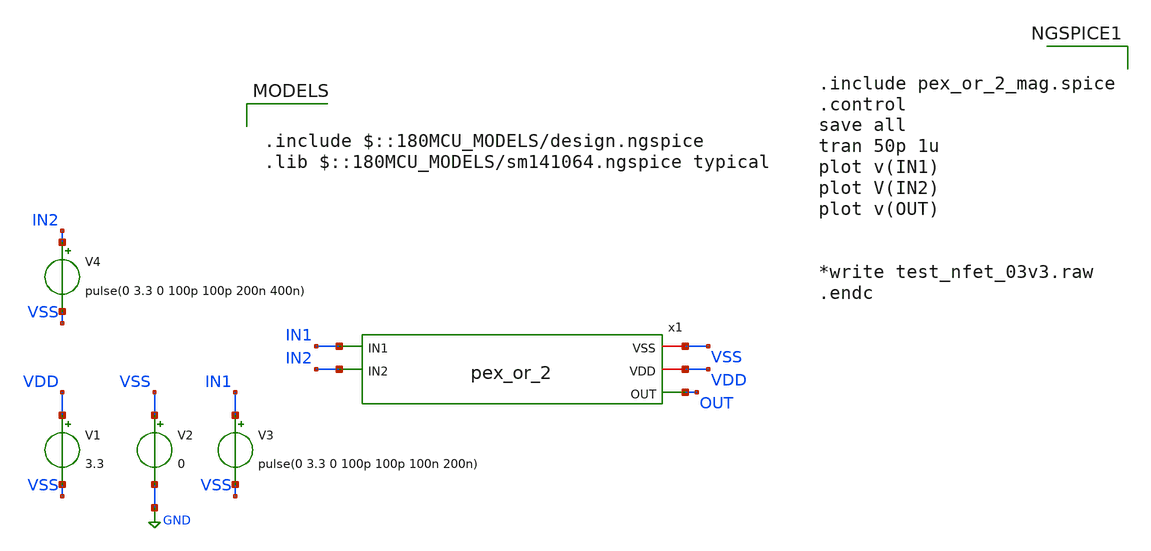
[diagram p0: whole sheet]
** sch_path: Clock_Generator_PAKISTAN_02/Schematics/pex_or_2_test.sch
**.subckt pex_or_2_test
V1 VDD VSS 3.3
V2 VSS GND 0
V3 IN1 VSS pulse(0 3.3 0 100p 100p 100n 200n)
V4 IN2 VSS pulse(0 3.3 0 100p 100p 200n 400n)
x1 IN1 VSS VDD OUT IN2 pex_or_2
**** begin user architecture code

.include $::180MCU_MODELS/design.ngspice
.lib $::180MCU_MODELS/sm141064.ngspice typical



.include pex_or_2_mag.spice
.control
save all
tran 50p 1u
plot v(IN1)
plot V(IN2)
plot v(OUT)


*write test_nfet_03v3.raw
.endc


**** end user architecture code
**.ends
.GLOBAL GND
.end
